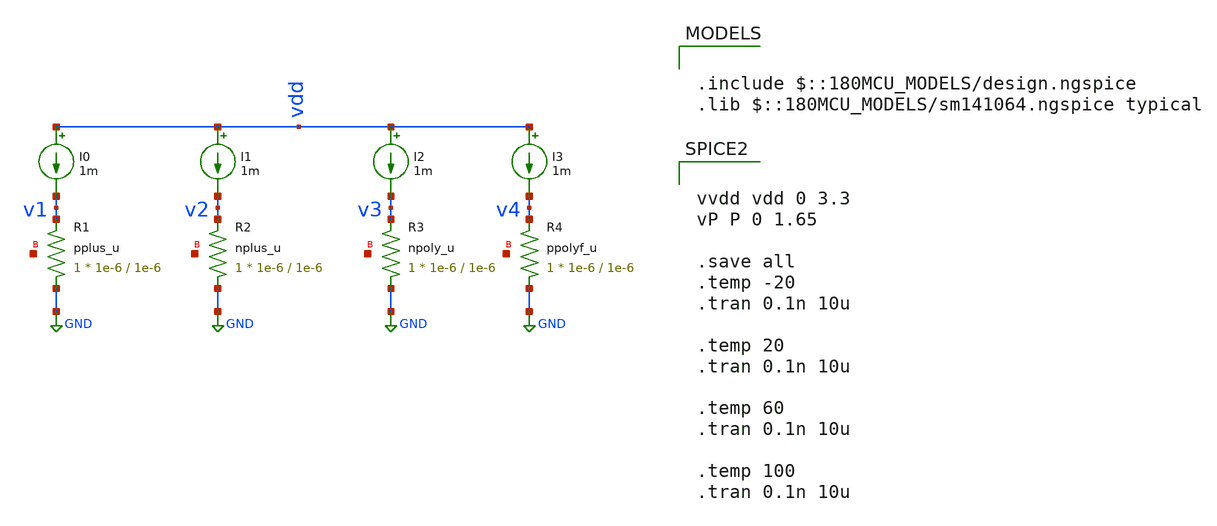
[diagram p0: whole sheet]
** sch_path: Clock_Reference/symbols_clock/ResistorTun.sch
**.subckt ResistorTun
XR1 GND v1 net1 pplus_u r_width=1e-6 r_length=1e-6 m=1
XR2 GND v2 net2 nplus_u r_width=1e-6 r_length=1e-6 m=1
XR4 GND v4 net3 ppolyf_u r_width=1e-6 r_length=1e-6 m=1
XR3 GND v3 net4 npoly_u r_width=1e-6 r_length=1e-6 m=1
I0 vdd v1 1m
I1 vdd v2 1m
I2 vdd v3 1m
I3 vdd v4 1m
**** begin user architecture code

.include $::180MCU_MODELS/design.ngspice
.lib $::180MCU_MODELS/sm141064.ngspice typical



vvdd vdd 0 3.3
vP P 0 1.65

.save all
.temp -20
.tran 0.1n 10u

.temp 20
.tran 0.1n 10u

.temp 60
.tran 0.1n 10u

.temp 100
.tran 0.1n 10u


**** end user architecture code
**.ends
.GLOBAL GND
.end
